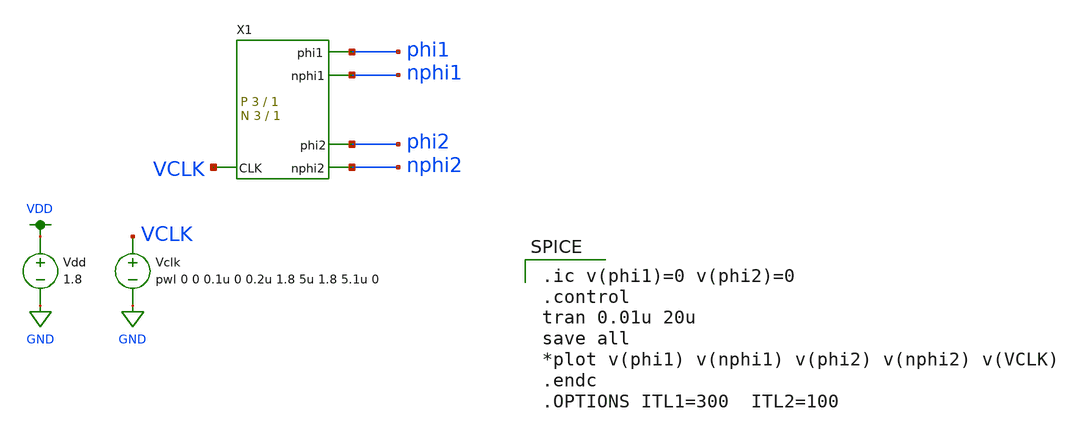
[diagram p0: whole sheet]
** sch_path: schematic/test/clk_gen_test.sch
**.subckt clk_gen_test
X1 phi1 phi2 VCLK nphi1 nphi2 clk_gen Wp=3 Lp=1 WW=3 LL=1
Vclk VCLK GND pwl 0 0 0.1u 0 0.2u 1.8 5u 1.8 5.1u 0
Vdd VDD GND 1.8
**** begin user architecture code

.option wnflag=1
.param MC_SWITCH=0.0
.lib ~/skywater/skywater-pdk/libraries/sky130_fd_pr_ngspice/latest/models/sky130.lib.spice tt


.ic v(phi1)=0 v(phi2)=0
.control
tran 0.01u 20u
save all
*plot v(phi1) v(nphi1) v(phi2) v(nphi2) v(VCLK)
.endc
.OPTIONS ITL1=300  ITL2=100

**** end user architecture code
**.ends
.GLOBAL GND
.GLOBAL VDD
.end
